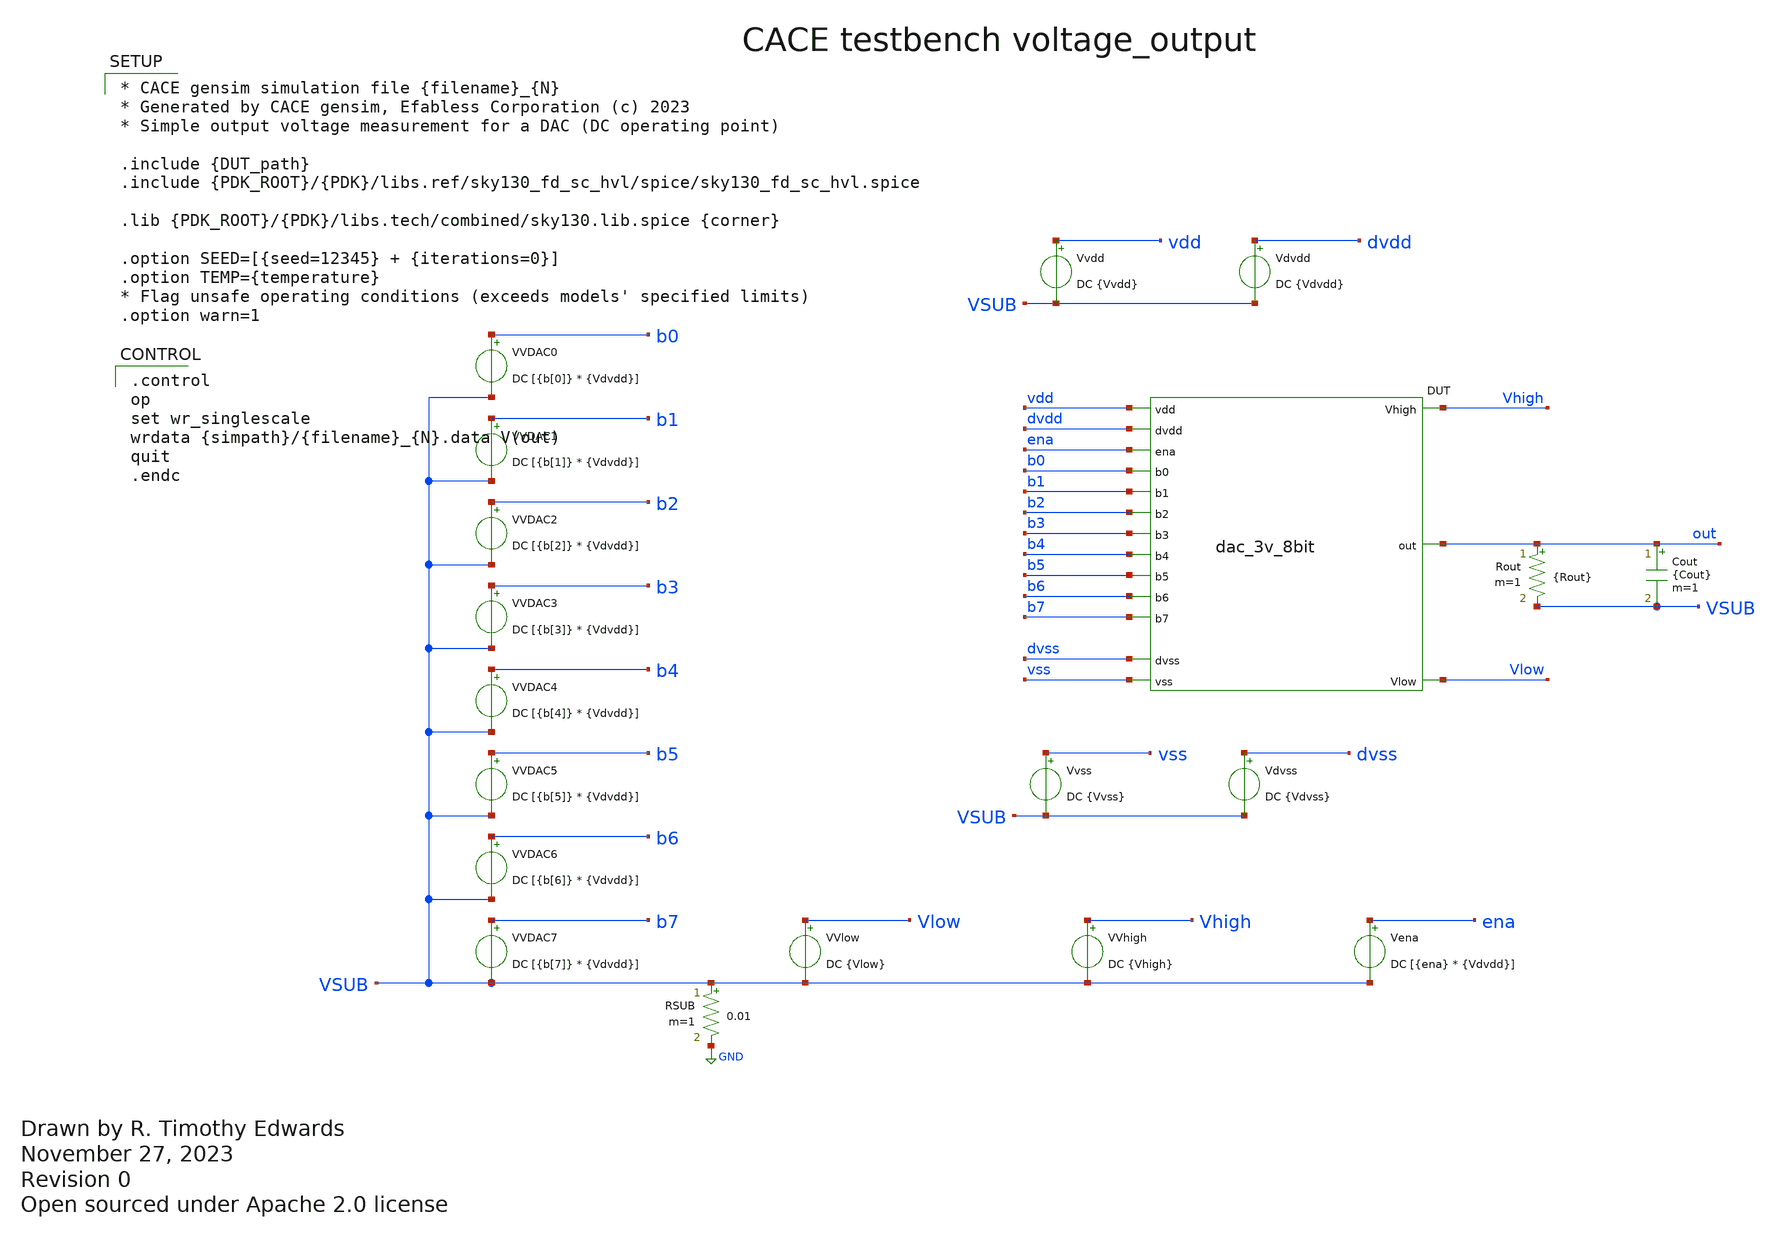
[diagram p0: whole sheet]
** sch_path: cace/voltage_output.sch
* Open sourced under Apache 2.0 license
**.subckt voltage_output
VVDAC7 b7 VSUB DC [{b[7]} * {Vdvdd}]
VVDAC1 b1 VSUB DC [{b[1]} * {Vdvdd}]
VVDAC2 b2 VSUB DC [{b[2]} * {Vdvdd}]
VVDAC3 b3 VSUB DC [{b[3]} * {Vdvdd}]
VVDAC4 b4 VSUB DC [{b[4]} * {Vdvdd}]
VVDAC5 b5 VSUB DC [{b[5]} * {Vdvdd}]
VVDAC6 b6 VSUB DC [{b[6]} * {Vdvdd}]
VVDAC0 b0 VSUB DC [{b[0]} * {Vdvdd}]
VVlow Vlow VSUB DC {Vlow}
VVhigh Vhigh VSUB DC {Vhigh}
Vena ena VSUB DC [{ena} * {Vdvdd}]
Vvss vss VSUB DC {Vvss}
Rout out VSUB {Rout} m=1
Cout out VSUB {Cout} m=1
Vdvss dvss VSUB DC {Vdvss}
Vvdd vdd VSUB DC {Vvdd}
Vdvdd dvdd VSUB DC {Vdvdd}
RSUB VSUB GND 0.01 m=1
XDUT {PIN|dvdd|dvdd} {PIN|vdd|vdd} {PIN|dvss|dvss} {PIN|vss|vss} {PIN|Vhigh|Vhigh} {PIN|Vlow|Vlow} {PIN|out|out}
+ {PIN|ena|ena} {PIN|b0|b0} {PIN|b1|b1} {PIN|b2|b2} {PIN|b3|b3} {PIN|b4|b4} {PIN|b5|b5} {PIN|b6|b6} {PIN|b7|b7}
+ {DUT_name}
**** begin user architecture code

.control
op
set wr_singlescale
wrdata {simpath}/{filename}_{N}.data V(out)
quit
.endc



* CACE gensim simulation file {filename}_{N}
* Generated by CACE gensim, Efabless Corporation (c) 2023
* Simple output voltage measurement for a DAC (DC operating point)

.include {DUT_path}
.include {PDK_ROOT}/{PDK}/libs.ref/sky130_fd_sc_hvl/spice/sky130_fd_sc_hvl.spice

.lib {PDK_ROOT}/{PDK}/libs.tech/combined/sky130.lib.spice {corner}

.option SEED=[{seed=12345} + {iterations=0}]
.option TEMP={temperature}
* Flag unsafe operating conditions (exceeds models' specified limits)
.option warn=1


**** end user architecture code
**.ends
.GLOBAL GND
.end
